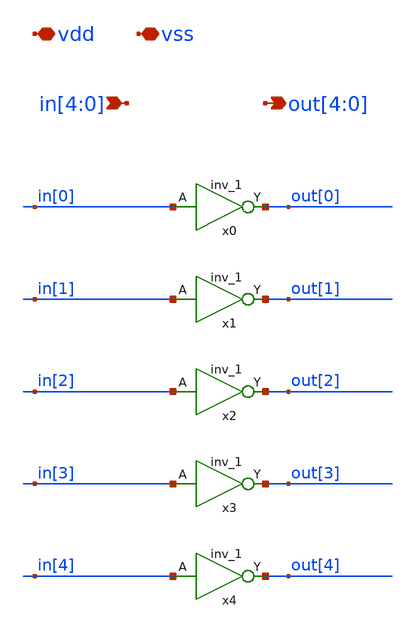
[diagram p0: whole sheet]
** sch_path: xschem/support/inv_5b.sch
**.subckt inv_5b out[4],out[3],out[2],out[1],out[0] vdd vss in[4],in[3],in[2],in[1],in[0]
*.opin out[4],out[3],out[2],out[1],out[0]
*.iopin vdd
*.iopin vss
*.ipin in[4],in[3],in[2],in[1],in[0]
x0 in[0] vss vss vdd vdd out[0] sky130_fd_sc_hd__inv_1
x1 in[1] vss vss vdd vdd out[1] sky130_fd_sc_hd__inv_1
x2 in[2] vss vss vdd vdd out[2] sky130_fd_sc_hd__inv_1
x3 in[3] vss vss vdd vdd out[3] sky130_fd_sc_hd__inv_1
x4 in[4] vss vss vdd vdd out[4] sky130_fd_sc_hd__inv_1
**.ends
.end
